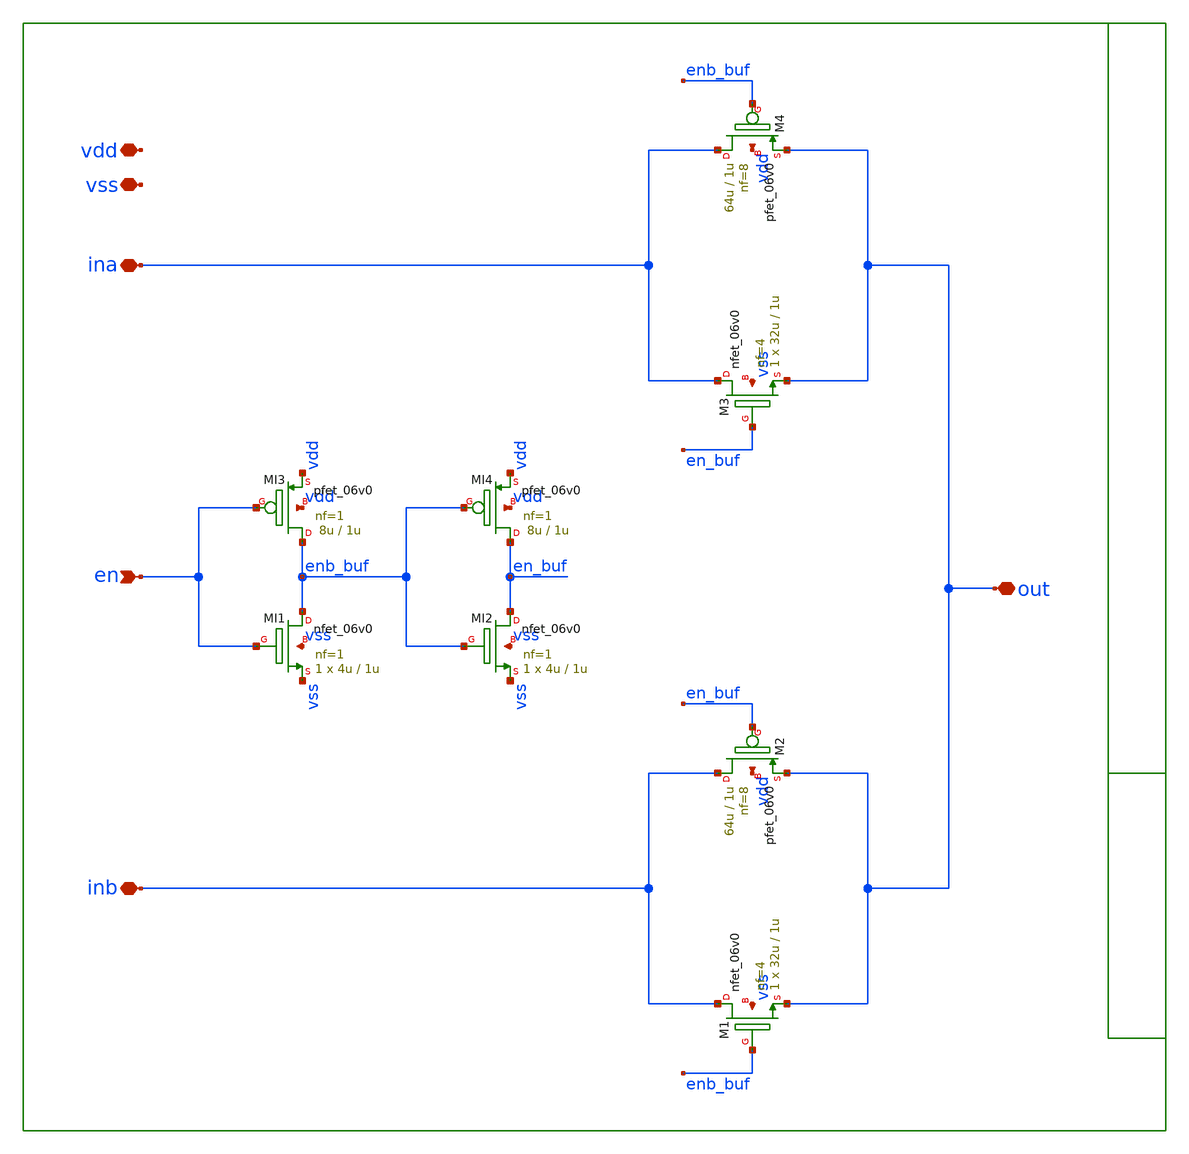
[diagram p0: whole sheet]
** sch_path: xschem/sch/spdt/spdt/spdt.sch
**.subckt spdt en vss vdd ina out inb
*.ipin en
*.iopin vss
*.iopin vdd
*.iopin ina
*.iopin out
*.iopin inb
XMI1 enb_buf en vss vss nfet_06v0 L=1u W=4u nf=1 ad='int((nf+1)/2) * W/nf * 0.18u' as='int((nf+2)/2) * W/nf * 0.18u'
+ pd='2*int((nf+1)/2) * (W/nf + 0.18u)' ps='2*int((nf+2)/2) * (W/nf + 0.18u)' nrd='0.18u / W' nrs='0.18u / W'
+ sa=0 sb=0 sd=0 m=1 par=1
XMI2 en_buf enb_buf vss vss nfet_06v0 L=1u W=4u nf=1 ad='int((nf+1)/2) * W/nf * 0.18u' as='int((nf+2)/2) * W/nf * 0.18u'
+ pd='2*int((nf+1)/2) * (W/nf + 0.18u)' ps='2*int((nf+2)/2) * (W/nf + 0.18u)' nrd='0.18u / W' nrs='0.18u / W'
+ sa=0 sb=0 sd=0 m=1 par=1
XMI3 enb_buf en vdd vdd pfet_06v0 L=1u W=8u nf=1 ad='int((nf+1)/2) * W/nf * 0.18u' as='int((nf+2)/2) * W/nf * 0.18u'
+ pd='2*int((nf+1)/2) * (W/nf + 0.18u)' ps='2*int((nf+2)/2) * (W/nf + 0.18u)' nrd='0.18u / W' nrs='0.18u / W'
+ sa=0 sb=0 sd=0 m=1 par=1
XMI4 en_buf enb_buf vdd vdd pfet_06v0 L=1u W=8u nf=1 ad='int((nf+1)/2) * W/nf * 0.18u' as='int((nf+2)/2) * W/nf * 0.18u'
+ pd='2*int((nf+1)/2) * (W/nf + 0.18u)' ps='2*int((nf+2)/2) * (W/nf + 0.18u)' nrd='0.18u / W' nrs='0.18u / W'
+ sa=0 sb=0 sd=0 m=1 par=1
XM2 inb en_buf out vdd pfet_06v0 L=1u W=64u nf=8 ad='int((nf+1)/2) * W/nf * 0.18u' as='int((nf+2)/2) * W/nf * 0.18u'
+ pd='2*int((nf+1)/2) * (W/nf + 0.18u)' ps='2*int((nf+2)/2) * (W/nf + 0.18u)' nrd='0.18u / W' nrs='0.18u / W'
+ sa=0 sb=0 sd=0 m=1 par=1
XM1 inb enb_buf out vss nfet_06v0 L=1u W=32u nf=4 ad='int((nf+1)/2) * W/nf * 0.18u' as='int((nf+2)/2) * W/nf * 0.18u'
+ pd='2*int((nf+1)/2) * (W/nf + 0.18u)' ps='2*int((nf+2)/2) * (W/nf + 0.18u)' nrd='0.18u / W' nrs='0.18u / W'
+ sa=0 sb=0 sd=0 m=1 par=1
XM3 ina en_buf out vss nfet_06v0 L=1u W=32u nf=4 ad='int((nf+1)/2) * W/nf * 0.18u' as='int((nf+2)/2) * W/nf * 0.18u'
+ pd='2*int((nf+1)/2) * (W/nf + 0.18u)' ps='2*int((nf+2)/2) * (W/nf + 0.18u)' nrd='0.18u / W' nrs='0.18u / W'
+ sa=0 sb=0 sd=0 m=1 par=1
XM4 ina enb_buf out vdd pfet_06v0 L=1u W=64u nf=8 ad='int((nf+1)/2) * W/nf * 0.18u' as='int((nf+2)/2) * W/nf * 0.18u'
+ pd='2*int((nf+1)/2) * (W/nf + 0.18u)' ps='2*int((nf+2)/2) * (W/nf + 0.18u)' nrd='0.18u / W' nrs='0.18u / W'
+ sa=0 sb=0 sd=0 m=1 par=1
**.ends
.end
